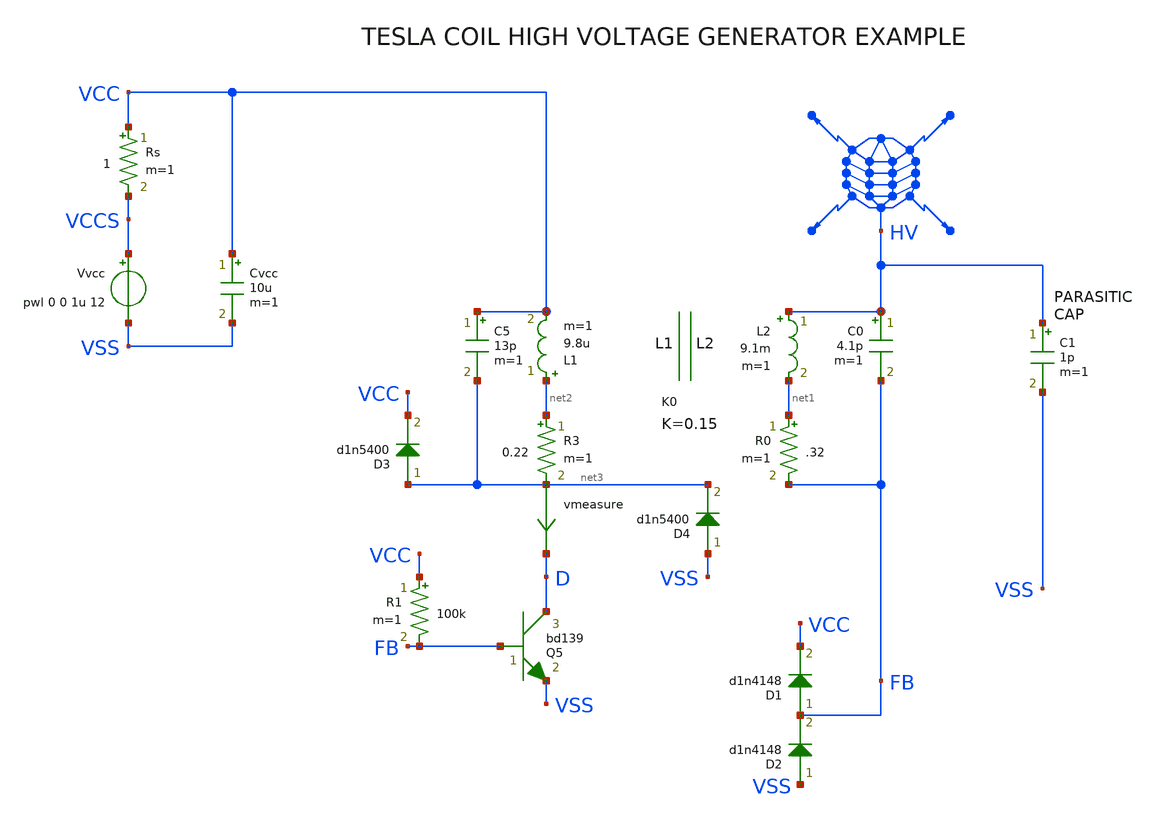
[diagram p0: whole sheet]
** sch_path: tests/test_sweep_diff/examples/tesla/schematic/tesla.sch
* Copyright (C) 1998-2024 Stefan Frederik Schippers
* This program is free software; you can redistribute it and/or modify
* it under the terms of the GNU General Public License as published by
* the Free Software Foundation; either version 2 of the License, or
* (at your option) any later version.
* This program is distributed in the hope that it will be useful,
* but WITHOUT ANY WARRANTY; without even the implied warranty of
* MERCHANTABILITY or FITNESS FOR A PARTICULAR PURPOSE.  See the
* GNU General Public License for more details.
* You should have received a copy of the GNU General Public License
* along with this program; if not, write to the Free Software
**.subckt tesla
Rs VCC VCCS 1 m=1
Vvcc VCCS VSS pwl 0 0 1u 12
Cvcc VCC VSS 10u m=1
C1 HV VSS 1p m=1
L1 net2 VCC 9.8u m=1
L2 HV net1 9.1m m=1
K0 L1 L2 0.15
R0 net1 FB .32 m=1
C0 HV FB 4.1p m=1
R3 net2 net3 0.22 m=1
C5 VCC net3 13p m=1
D2 VSS FB d1n4148 area=1
D1 FB VCC d1n4148 area=1
Q5 D FB VSS bd139 area=1 m=1
R1 VCC FB 100k m=1
D3 net3 VCC d1n5400 area=1
vmeasure net3 D 0
.save i(vmeasure)
D4 VSS net3 d1n5400 area=1
**** begin user architecture code

.option SCALE=1e-6 PARHIER=LOCAL RUNLVL=6 post MODMONTE=1
.option sampling_method = SRS
.option method=gear savecurrents
vvss vss 0 dc 0

.save all
.save tran @q5[p]
** models are generally not free: you must download
** SPICE models for active devices and put them  into the below
** referenced file in simulation directory.
.include models_tesla.txt
.temp 30

.control
tran 40n 1m  uic
meas tran iavg AVG i(vvcc) from=950u to=990u
save tran p(q5) i(l1) i(l2)
write tesla.raw
quit 0
.endc


**** end user architecture code
**.ends
.end
